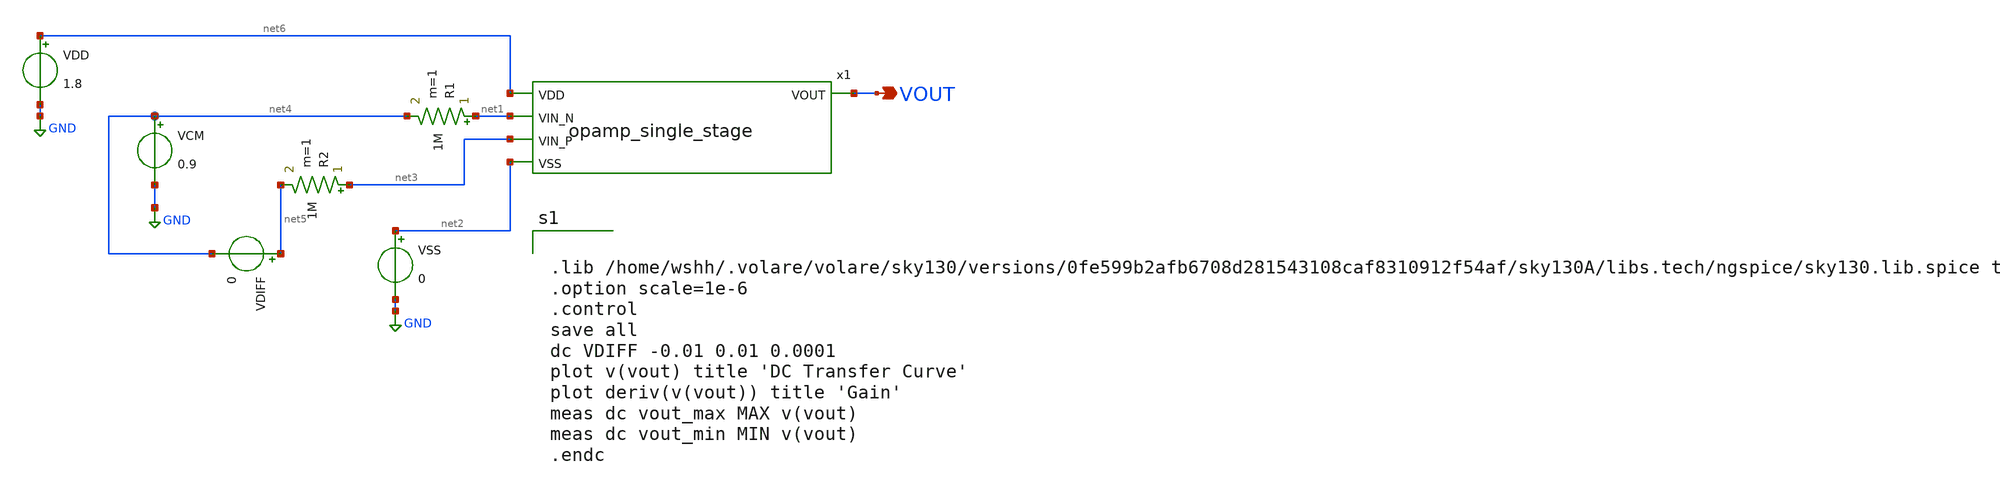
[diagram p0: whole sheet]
** sch_path: analog/schematics/ tb_dc_gain.sch
**.subckt  tb_dc_gain VOUT
*.opin VOUT
VSS net2 GND 0
VDD net6 GND 1.8
VCM net4 GND 0.9
VDIFF net5 net4 0
R1 net1 net4 1M m=1
R2 net3 net5 1M m=1
x1 net6 VOUT net1 net3 net2 opamp_single_stage
**** begin user architecture code


.lib /home/wshh/.volare/volare/sky130/versions/0fe599b2afb6708d281543108caf8310912f54af/sky130A/libs.tech/ngspice/sky130.lib.spice tt
.option scale=1e-6
.control
save all
dc VDIFF -0.01 0.01 0.0001
plot v(vout) title 'DC Transfer Curve'
plot deriv(v(vout)) title 'Gain'
meas dc vout_max MAX v(vout)
meas dc vout_min MIN v(vout)
.endc


**** end user architecture code
**.ends

* expanding   symbol:  opamp_single_stage.sym # of pins=5
** sym_path: analog/schematics/opamp_single_stage.sym
** sch_path: analog/schematics/opamp_single_stage.sch
.subckt opamp_single_stage VDD VOUT VIN_N VIN_P VSS
*.ipin VIN_P
*.ipin VIN_N
*.ipin VDD
*.ipin VSS
*.opin VOUT
XM3 VDD net1 net1 VDD sky130_fd_pr__pfet_01v8 L=0.5 W=5 nf=1 ad='int((nf+1)/2) * W/nf * 0.29' as='int((nf+2)/2) * W/nf * 0.29'
+ pd='2*int((nf+1)/2) * (W/nf + 0.29)' ps='2*int((nf+2)/2) * (W/nf + 0.29)' nrd='0.29 / W' nrs='0.29 / W'
+ sa=0 sb=0 sd=0 mult=1 m=1
XM4 net2 net1 VDD VDD sky130_fd_pr__pfet_01v8 L=0.5 W=5 nf=1 ad='int((nf+1)/2) * W/nf * 0.29' as='int((nf+2)/2) * W/nf * 0.29'
+ pd='2*int((nf+1)/2) * (W/nf + 0.29)' ps='2*int((nf+2)/2) * (W/nf + 0.29)' nrd='0.29 / W' nrs='0.29 / W'
+ sa=0 sb=0 sd=0 mult=1 m=1
VB2 net5 GND 0.7
XM1 net1 VIN_P net3 GND sky130_fd_pr__nfet_01v8 L=0.5 W=5 nf=1 ad='int((nf+1)/2) * W/nf * 0.29' as='int((nf+2)/2) * W/nf * 0.29'
+ pd='2*int((nf+1)/2) * (W/nf + 0.29)' ps='2*int((nf+2)/2) * (W/nf + 0.29)' nrd='0.29 / W' nrs='0.29 / W'
+ sa=0 sb=0 sd=0 mult=1 m=1
XM2 net3 VIN_N net2 GND sky130_fd_pr__nfet_01v8 L=0.5 W=5 nf=1 ad='int((nf+1)/2) * W/nf * 0.29' as='int((nf+2)/2) * W/nf * 0.29'
+ pd='2*int((nf+1)/2) * (W/nf + 0.29)' ps='2*int((nf+2)/2) * (W/nf + 0.29)' nrd='0.29 / W' nrs='0.29 / W'
+ sa=0 sb=0 sd=0 mult=1 m=1
XM9 VSS net5 net3 GND sky130_fd_pr__nfet_01v8 L=0.5 W=5 nf=1 ad='int((nf+1)/2) * W/nf * 0.29' as='int((nf+2)/2) * W/nf * 0.29'
+ pd='2*int((nf+1)/2) * (W/nf + 0.29)' ps='2*int((nf+2)/2) * (W/nf + 0.29)' nrd='0.29 / W' nrs='0.29 / W'
+ sa=0 sb=0 sd=0 mult=1 m=1
XM5 VOUT_S2 net2 VDD VDD sky130_fd_pr__pfet_01v8 L=0.5 W=5 nf=1 ad='int((nf+1)/2) * W/nf * 0.29' as='int((nf+2)/2) * W/nf * 0.29'
+ pd='2*int((nf+1)/2) * (W/nf + 0.29)' ps='2*int((nf+2)/2) * (W/nf + 0.29)' nrd='0.29 / W' nrs='0.29 / W'
+ sa=0 sb=0 sd=0 mult=1 m=1
XM6 VOUT_S2 net5 VSS GND sky130_fd_pr__nfet_01v8 L=0.5 W=5 nf=1 ad='int((nf+1)/2) * W/nf * 0.29' as='int((nf+2)/2) * W/nf * 0.29'
+ pd='2*int((nf+1)/2) * (W/nf + 0.29)' ps='2*int((nf+2)/2) * (W/nf + 0.29)' nrd='0.29 / W' nrs='0.29 / W'
+ sa=0 sb=0 sd=0 mult=1 m=1
R1 net2 net4 5k m=1
C1 net4 VOUT_S2 2p m=1
XM7 VOUT VOUT_S2 VDD VDD sky130_fd_pr__pfet_01v8 L=0.5 W=10 nf=1 ad='int((nf+1)/2) * W/nf * 0.29' as='int((nf+2)/2) * W/nf * 0.29'
+ pd='2*int((nf+1)/2) * (W/nf + 0.29)' ps='2*int((nf+2)/2) * (W/nf + 0.29)' nrd='0.29 / W' nrs='0.29 / W'
+ sa=0 sb=0 sd=0 mult=1 m=1
XM8 VOUT VOUT_S2 VSS GND sky130_fd_pr__nfet_01v8 L=0.5 W=10 nf=1 ad='int((nf+1)/2) * W/nf * 0.29' as='int((nf+2)/2) * W/nf * 0.29'
+ pd='2*int((nf+1)/2) * (W/nf + 0.29)' ps='2*int((nf+2)/2) * (W/nf + 0.29)' nrd='0.29 / W' nrs='0.29 / W'
+ sa=0 sb=0 sd=0 mult=1 m=1
.ends

.GLOBAL GND
.end
